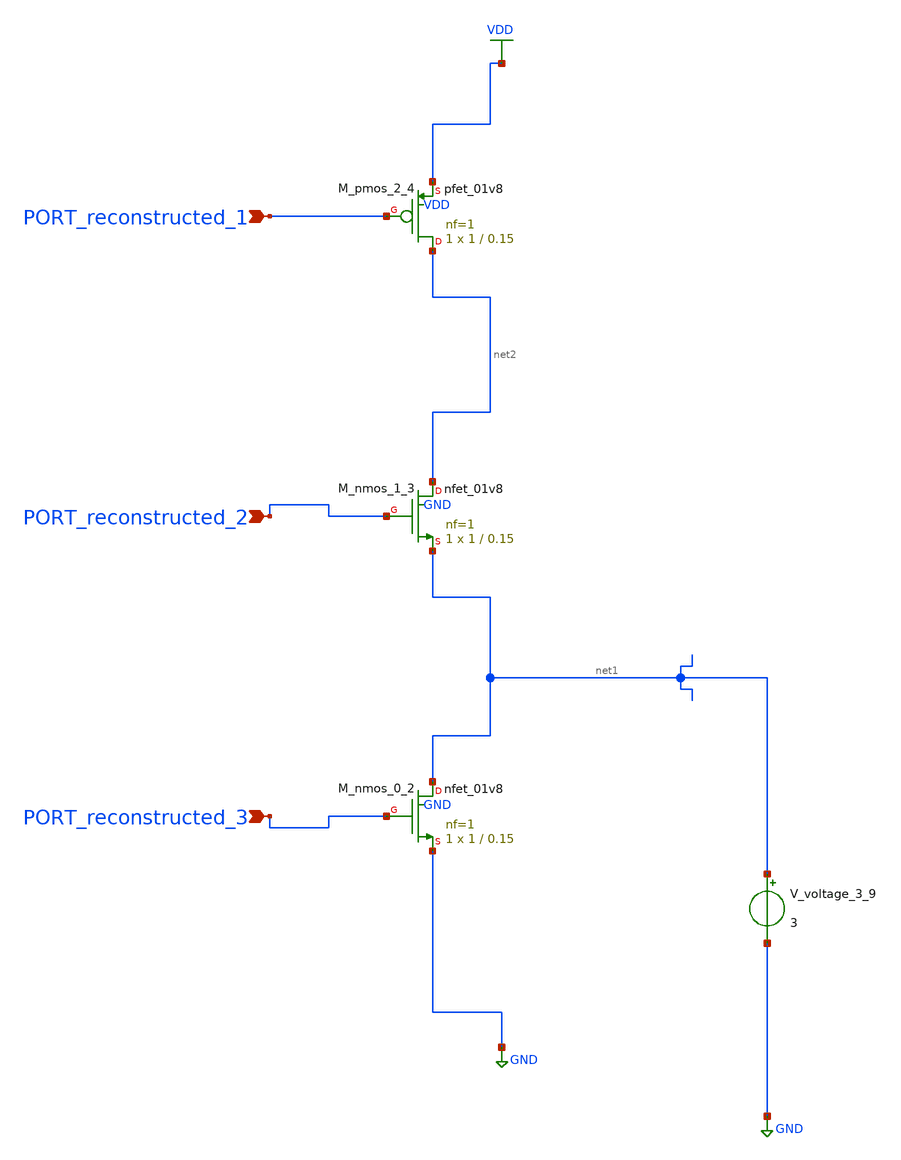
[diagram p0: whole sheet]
** sch_path: schematics/AMSNet/163.sch
**.subckt 163 PORT_reconstructed_2 PORT_reconstructed_3 PORT_reconstructed_1
*.ipin PORT_reconstructed_2
*.ipin PORT_reconstructed_3
*.ipin PORT_reconstructed_1
XM_nmos_0_2 net1 PORT_reconstructed_3 GND GND sky130_fd_pr__nfet_01v8 L=0.15 W=1 nf=1 ad='int((1 + 1)/2) * 1 / 1 * 0.29'
+ as='int((1 + 2)/2) * 1 / 1 * 0.29' pd='2*int((1 + 1)/2) * (1 / 1 + 0.29)' ps='2*int((1 + 2)/2) * (1 / 1 + 0.29)'
+ nrd='0.29 / 1 ' nrs='0.29 / 1 ' sa=0 sb=0 sd=0 mult=1 m=1
XM_nmos_1_3 net2 PORT_reconstructed_2 net1 GND sky130_fd_pr__nfet_01v8 L=0.15 W=1 nf=1 ad='int((1 + 1)/2) * 1 / 1 * 0.29'
+ as='int((1 + 2)/2) * 1 / 1 * 0.29' pd='2*int((1 + 1)/2) * (1 / 1 + 0.29)' ps='2*int((1 + 2)/2) * (1 / 1 + 0.29)'
+ nrd='0.29 / 1 ' nrs='0.29 / 1 ' sa=0 sb=0 sd=0 mult=1 m=1
XM_pmos_2_4 net2 PORT_reconstructed_1 VDD VDD sky130_fd_pr__pfet_01v8 L=0.15 W=1 nf=1 ad='int((1 + 1)/2) * 1 / 1 * 0.29'
+ as='int((1 + 2)/2) * 1 / 1 * 0.29' pd='2*int((1 + 1)/2) * (1 / 1 + 0.29)' ps='2*int((1 + 2)/2) * (1 / 1 + 0.29)'
+ nrd='0.29 / 1 ' nrs='0.29 / 1 ' sa=0 sb=0 sd=0 mult=1 m=1
V_voltage_3_9 net1 GND 3
**.ends
.GLOBAL GND
.GLOBAL VDD
.end
